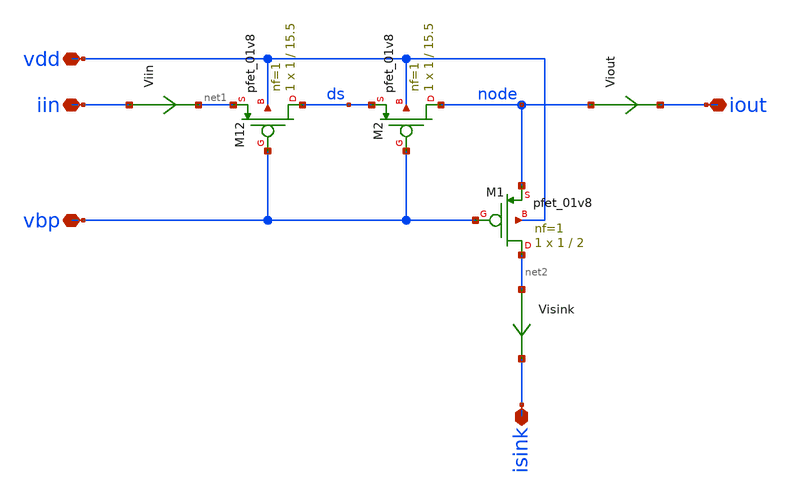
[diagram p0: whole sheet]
** sch_path: xschem/divider.sch
**.subckt divider iin vdd vbp iout isink
*.iopin iin
*.iopin vdd
*.iopin vbp
*.iopin iout
*.iopin isink
XM12 ds vbp net1 vdd sky130_fd_pr__pfet_01v8 L=15.5 W=1 nf=1 ad='int((nf+1)/2) * W/nf * 0.29' as='int((nf+2)/2) * W/nf * 0.29'
+ pd='2*int((nf+1)/2) * (W/nf + 0.29)' ps='2*int((nf+2)/2) * (W/nf + 0.29)' nrd='0.29 / W' nrs='0.29 / W'
+ sa=0 sb=0 sd=0 mult=1 m=1
Viin iin net1 0
.save i(viin)
Viout node iout 0
.save i(viout)
XM1 net2 vbp node vdd sky130_fd_pr__pfet_01v8 L=2 W=1 nf=1 ad='int((nf+1)/2) * W/nf * 0.29' as='int((nf+2)/2) * W/nf * 0.29'
+ pd='2*int((nf+1)/2) * (W/nf + 0.29)' ps='2*int((nf+2)/2) * (W/nf + 0.29)' nrd='0.29 / W' nrs='0.29 / W'
+ sa=0 sb=0 sd=0 mult=1 m=1
Visink net2 isink 0
.save i(visink)
XM2 node vbp ds vdd sky130_fd_pr__pfet_01v8 L=15.5 W=1 nf=1 ad='int((nf+1)/2) * W/nf * 0.29' as='int((nf+2)/2) * W/nf * 0.29'
+ pd='2*int((nf+1)/2) * (W/nf + 0.29)' ps='2*int((nf+2)/2) * (W/nf + 0.29)' nrd='0.29 / W' nrs='0.29 / W'
+ sa=0 sb=0 sd=0 mult=1 m=1
**.ends
.end
